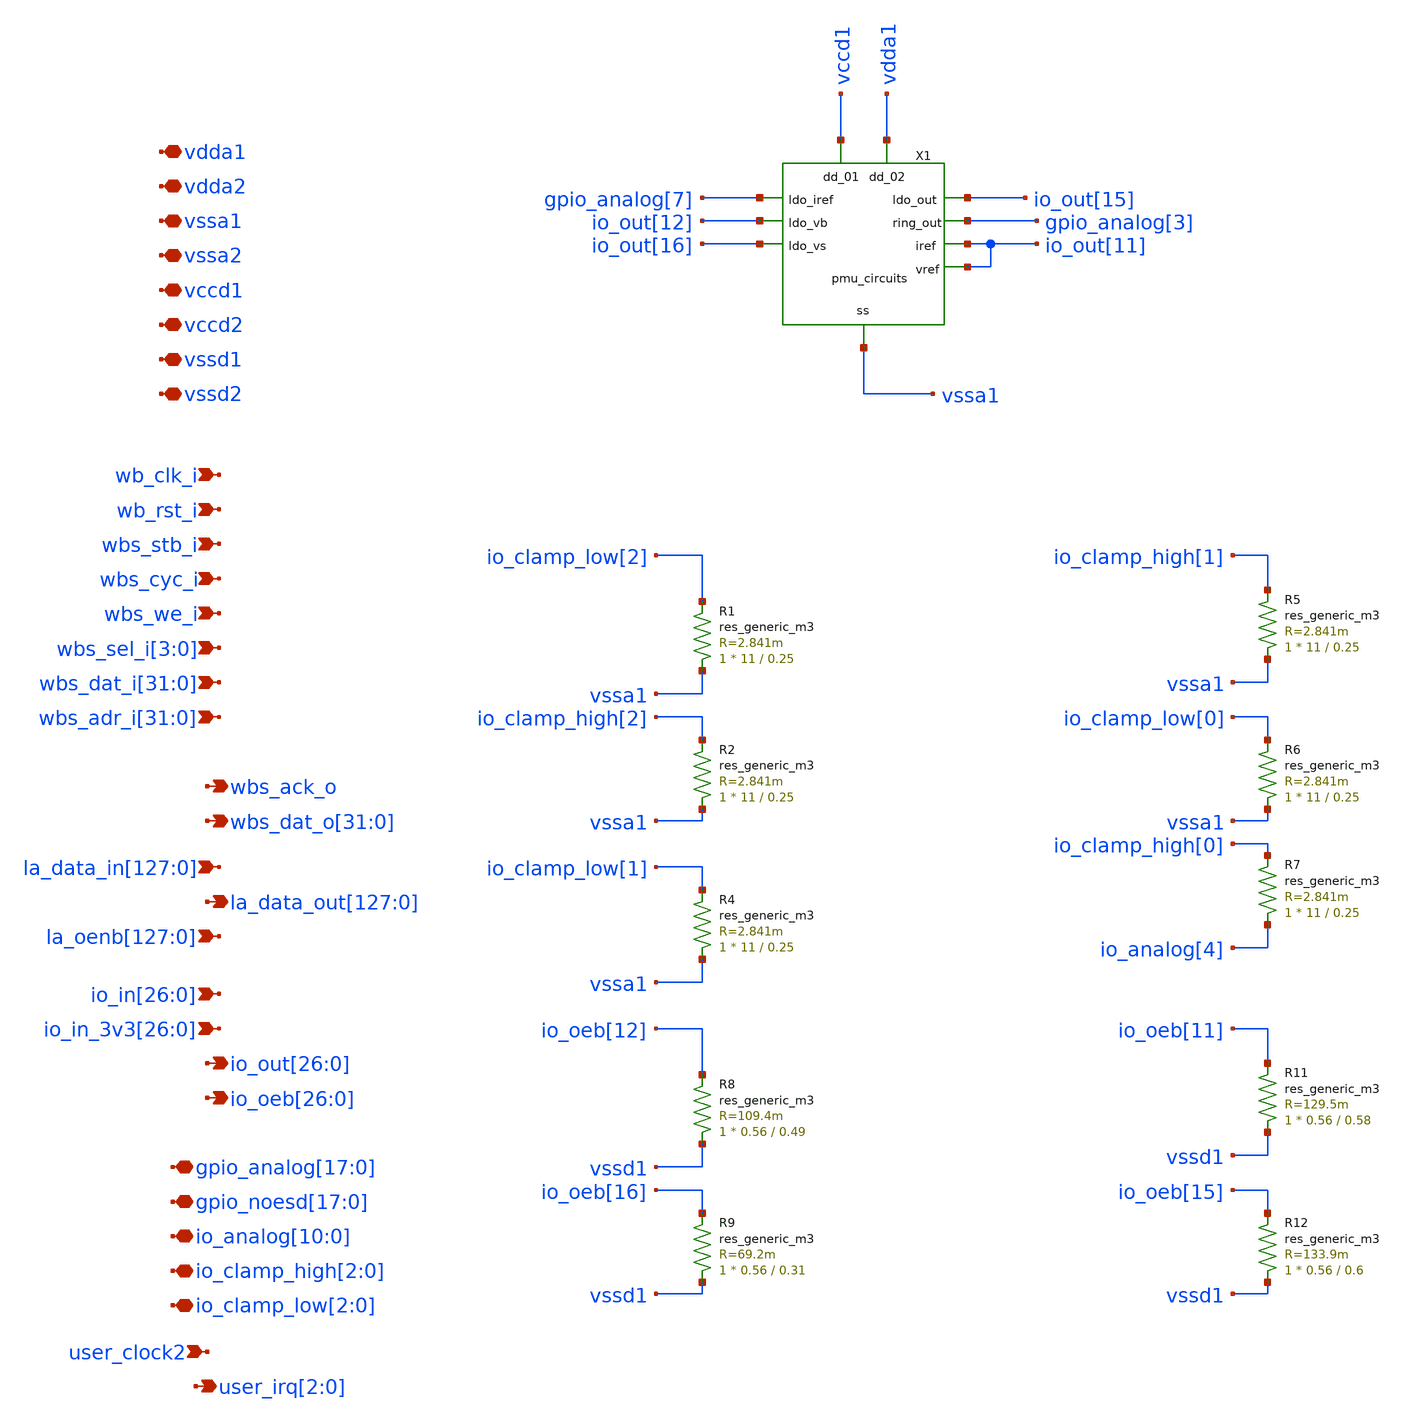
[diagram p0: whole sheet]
** sch_path: xschem/user_analog_project_wrapper.sch
**.subckt user_analog_project_wrapper vdda1 vdda2 vssa1 vssa2 vccd1 vccd2 vssd1 vssd2 wb_clk_i
*+ wb_rst_i wbs_stb_i wbs_cyc_i wbs_we_i wbs_sel_i[3],wbs_sel_i[2],wbs_sel_i[1],wbs_sel_i[0]
*+ wbs_dat_i[31],wbs_dat_i[30],wbs_dat_i[29],wbs_dat_i[28],wbs_dat_i[27],wbs_dat_i[26],wbs_dat_i[25],wbs_dat_i[24],wbs_dat_i[23],wbs_dat_i[22],wbs_dat_i[21],wbs_dat_i[20],wbs_dat_i[19],wbs_dat_i[18],wbs_dat_i[17],wbs_dat_i[16],wbs_dat_i[15],wbs_dat_i[14],wbs_dat_i[13],wbs_dat_i[12],wbs_dat_i[11],wbs_dat_i[10],wbs_dat_i[9],wbs_dat_i[8],wbs_dat_i[7],wbs_dat_i[6],wbs_dat_i[5],wbs_dat_i[4],wbs_dat_i[3],wbs_dat_i[2],wbs_dat_i[1],wbs_dat_i[0]
*+ wbs_adr_i[31],wbs_adr_i[30],wbs_adr_i[29],wbs_adr_i[28],wbs_adr_i[27],wbs_adr_i[26],wbs_adr_i[25],wbs_adr_i[24],wbs_adr_i[23],wbs_adr_i[22],wbs_adr_i[21],wbs_adr_i[20],wbs_adr_i[19],wbs_adr_i[18],wbs_adr_i[17],wbs_adr_i[16],wbs_adr_i[15],wbs_adr_i[14],wbs_adr_i[13],wbs_adr_i[12],wbs_adr_i[11],wbs_adr_i[10],wbs_adr_i[9],wbs_adr_i[8],wbs_adr_i[7],wbs_adr_i[6],wbs_adr_i[5],wbs_adr_i[4],wbs_adr_i[3],wbs_adr_i[2],wbs_adr_i[1],wbs_adr_i[0] wbs_ack_o
*+ wbs_dat_o[31],wbs_dat_o[30],wbs_dat_o[29],wbs_dat_o[28],wbs_dat_o[27],wbs_dat_o[26],wbs_dat_o[25],wbs_dat_o[24],wbs_dat_o[23],wbs_dat_o[22],wbs_dat_o[21],wbs_dat_o[20],wbs_dat_o[19],wbs_dat_o[18],wbs_dat_o[17],wbs_dat_o[16],wbs_dat_o[15],wbs_dat_o[14],wbs_dat_o[13],wbs_dat_o[12],wbs_dat_o[11],wbs_dat_o[10],wbs_dat_o[9],wbs_dat_o[8],wbs_dat_o[7],wbs_dat_o[6],wbs_dat_o[5],wbs_dat_o[4],wbs_dat_o[3],wbs_dat_o[2],wbs_dat_o[1],wbs_dat_o[0]
*+ la_data_in[127],la_data_in[126],la_data_in[125],la_data_in[124],la_data_in[123],la_data_in[122],la_data_in[121],la_data_in[120],la_data_in[119],la_data_in[118],la_data_in[117],la_data_in[116],la_data_in[115],la_data_in[114],la_data_in[113],la_data_in[112],la_data_in[111],la_data_in[110],la_data_in[109],la_data_in[108],la_data_in[107],la_data_in[106],la_data_in[105],la_data_in[104],la_data_in[103],la_data_in[102],la_data_in[101],la_data_in[100],la_data_in[99],la_data_in[98],la_data_in[97],la_data_in[96],la_data_in[95],la_data_in[94],la_data_in[93],la_data_in[92],la_data_in[91],la_data_in[90],la_data_in[89],la_data_in[88],la_data_in[87],la_data_in[86],la_data_in[85],la_data_in[84],la_data_in[83],la_data_in[82],la_data_in[81],la_data_in[80],la_data_in[79],la_data_in[78],la_data_in[77],la_data_in[76],la_data_in[75],la_data_in[74],la_data_in[73],la_data_in[72],la_data_in[71],la_data_in[70],la_data_in[69],la_data_in[68],la_data_in[67],la_data_in[66],la_data_in[65],la_data_in[64],la_data_in[63],la_data_in[62],la_data_in[61],la_data_in[60],la_data_in[59],la_data_in[58],la_data_in[57],la_data_in[56],la_data_in[55],la_data_in[54],la_data_in[53],la_data_in[52],la_data_in[51],la_data_in[50],la_data_in[49],la_data_in[48],la_data_in[47],la_data_in[46],la_data_in[45],la_data_in[44],la_data_in[43],la_data_in[42],la_data_in[41],la_data_in[40],la_data_in[39],la_data_in[38],la_data_in[37],la_data_in[36],la_data_in[35],la_data_in[34],la_data_in[33],la_data_in[32],la_data_in[31],la_data_in[30],la_data_in[29],la_data_in[28],la_data_in[27],la_data_in[26],la_data_in[25],la_data_in[24],la_data_in[23],la_data_in[22],la_data_in[21],la_data_in[20],la_data_in[19],la_data_in[18],la_data_in[17],la_data_in[16],la_data_in[15],la_data_in[14],la_data_in[13],la_data_in[12],la_data_in[11],la_data_in[10],la_data_in[9],la_data_in[8],la_data_in[7],la_data_in[6],la_data_in[5],la_data_in[4],la_data_in[3],la_data_in[2],la_data_in[1],la_data_in[0]
*+ la_data_out[127],la_data_out[126],la_data_out[125],la_data_out[124],la_data_out[123],la_data_out[122],la_data_out[121],la_data_out[120],la_data_out[119],la_data_out[118],la_data_out[117],la_data_out[116],la_data_out[115],la_data_out[114],la_data_out[113],la_data_out[112],la_data_out[111],la_data_out[110],la_data_out[109],la_data_out[108],la_data_out[107],la_data_out[106],la_data_out[105],la_data_out[104],la_data_out[103],la_data_out[102],la_data_out[101],la_data_out[100],la_data_out[99],la_data_out[98],la_data_out[97],la_data_out[96],la_data_out[95],la_data_out[94],la_data_out[93],la_data_out[92],la_data_out[91],la_data_out[90],la_data_out[89],la_data_out[88],la_data_out[87],la_data_out[86],la_data_out[85],la_data_out[84],la_data_out[83],la_data_out[82],la_data_out[81],la_data_out[80],la_data_out[79],la_data_out[78],la_data_out[77],la_data_out[76],la_data_out[75],la_data_out[74],la_data_out[73],la_data_out[72],la_data_out[71],la_data_out[70],la_data_out[69],la_data_out[68],la_data_out[67],la_data_out[66],la_data_out[65],la_data_out[64],la_data_out[63],la_data_out[62],la_data_out[61],la_data_out[60],la_data_out[59],la_data_out[58],la_data_out[57],la_data_out[56],la_data_out[55],la_data_out[54],la_data_out[53],la_data_out[52],la_data_out[51],la_data_out[50],la_data_out[49],la_data_out[48],la_data_out[47],la_data_out[46],la_data_out[45],la_data_out[44],la_data_out[43],la_data_out[42],la_data_out[41],la_data_out[40],la_data_out[39],la_data_out[38],la_data_out[37],la_data_out[36],la_data_out[35],la_data_out[34],la_data_out[33],la_data_out[32],la_data_out[31],la_data_out[30],la_data_out[29],la_data_out[28],la_data_out[27],la_data_out[26],la_data_out[25],la_data_out[24],la_data_out[23],la_data_out[22],la_data_out[21],la_data_out[20],la_data_out[19],la_data_out[18],la_data_out[17],la_data_out[16],la_data_out[15],la_data_out[14],la_data_out[13],la_data_out[12],la_data_out[11],la_data_out[10],la_data_out[9],la_data_out[8],la_data_out[7],la_data_out[6],la_data_out[5],la_data_out[4],la_data_out[3],la_data_out[2],la_data_out[1],la_data_out[0]
*+ io_in[26],io_in[25],io_in[24],io_in[23],io_in[22],io_in[21],io_in[20],io_in[19],io_in[18],io_in[17],io_in[16],io_in[15],io_in[14],io_in[13],io_in[12],io_in[11],io_in[10],io_in[9],io_in[8],io_in[7],io_in[6],io_in[5],io_in[4],io_in[3],io_in[2],io_in[1],io_in[0]
*+ io_in_3v3[26],io_in_3v3[25],io_in_3v3[24],io_in_3v3[23],io_in_3v3[22],io_in_3v3[21],io_in_3v3[20],io_in_3v3[19],io_in_3v3[18],io_in_3v3[17],io_in_3v3[16],io_in_3v3[15],io_in_3v3[14],io_in_3v3[13],io_in_3v3[12],io_in_3v3[11],io_in_3v3[10],io_in_3v3[9],io_in_3v3[8],io_in_3v3[7],io_in_3v3[6],io_in_3v3[5],io_in_3v3[4],io_in_3v3[3],io_in_3v3[2],io_in_3v3[1],io_in_3v3[0] user_clock2
*+ io_out[26],io_out[25],io_out[24],io_out[23],io_out[22],io_out[21],io_out[20],io_out[19],io_out[18],io_out[17],io_out[16],io_out[15],io_out[14],io_out[13],io_out[12],io_out[11],io_out[10],io_out[9],io_out[8],io_out[7],io_out[6],io_out[5],io_out[4],io_out[3],io_out[2],io_out[1],io_out[0]
*+ io_oeb[26],io_oeb[25],io_oeb[24],io_oeb[23],io_oeb[22],io_oeb[21],io_oeb[20],io_oeb[19],io_oeb[18],io_oeb[17],io_oeb[16],io_oeb[15],io_oeb[14],io_oeb[13],io_oeb[12],io_oeb[11],io_oeb[10],io_oeb[9],io_oeb[8],io_oeb[7],io_oeb[6],io_oeb[5],io_oeb[4],io_oeb[3],io_oeb[2],io_oeb[1],io_oeb[0]
*+ gpio_analog[17],gpio_analog[16],gpio_analog[15],gpio_analog[14],gpio_analog[13],gpio_analog[12],gpio_analog[11],gpio_analog[10],gpio_analog[9],gpio_analog[8],gpio_analog[7],gpio_analog[6],gpio_analog[5],gpio_analog[4],gpio_analog[3],gpio_analog[2],gpio_analog[1],gpio_analog[0]
*+ gpio_noesd[17],gpio_noesd[16],gpio_noesd[15],gpio_noesd[14],gpio_noesd[13],gpio_noesd[12],gpio_noesd[11],gpio_noesd[10],gpio_noesd[9],gpio_noesd[8],gpio_noesd[7],gpio_noesd[6],gpio_noesd[5],gpio_noesd[4],gpio_noesd[3],gpio_noesd[2],gpio_noesd[1],gpio_noesd[0]
*+ io_analog[10],io_analog[9],io_analog[8],io_analog[7],io_analog[6],io_analog[5],io_analog[4],io_analog[3],io_analog[2],io_analog[1],io_analog[0] io_clamp_high[2],io_clamp_high[1],io_clamp_high[0] io_clamp_low[2],io_clamp_low[1],io_clamp_low[0]
*+ user_irq[2],user_irq[1],user_irq[0]
*+ la_oenb[127],la_oenb[126],la_oenb[125],la_oenb[124],la_oenb[123],la_oenb[122],la_oenb[121],la_oenb[120],la_oenb[119],la_oenb[118],la_oenb[117],la_oenb[116],la_oenb[115],la_oenb[114],la_oenb[113],la_oenb[112],la_oenb[111],la_oenb[110],la_oenb[109],la_oenb[108],la_oenb[107],la_oenb[106],la_oenb[105],la_oenb[104],la_oenb[103],la_oenb[102],la_oenb[101],la_oenb[100],la_oenb[99],la_oenb[98],la_oenb[97],la_oenb[96],la_oenb[95],la_oenb[94],la_oenb[93],la_oenb[92],la_oenb[91],la_oenb[90],la_oenb[89],la_oenb[88],la_oenb[87],la_oenb[86],la_oenb[85],la_oenb[84],la_oenb[83],la_oenb[82],la_oenb[81],la_oenb[80],la_oenb[79],la_oenb[78],la_oenb[77],la_oenb[76],la_oenb[75],la_oenb[74],la_oenb[73],la_oenb[72],la_oenb[71],la_oenb[70],la_oenb[69],la_oenb[68],la_oenb[67],la_oenb[66],la_oenb[65],la_oenb[64],la_oenb[63],la_oenb[62],la_oenb[61],la_oenb[60],la_oenb[59],la_oenb[58],la_oenb[57],la_oenb[56],la_oenb[55],la_oenb[54],la_oenb[53],la_oenb[52],la_oenb[51],la_oenb[50],la_oenb[49],la_oenb[48],la_oenb[47],la_oenb[46],la_oenb[45],la_oenb[44],la_oenb[43],la_oenb[42],la_oenb[41],la_oenb[40],la_oenb[39],la_oenb[38],la_oenb[37],la_oenb[36],la_oenb[35],la_oenb[34],la_oenb[33],la_oenb[32],la_oenb[31],la_oenb[30],la_oenb[29],la_oenb[28],la_oenb[27],la_oenb[26],la_oenb[25],la_oenb[24],la_oenb[23],la_oenb[22],la_oenb[21],la_oenb[20],la_oenb[19],la_oenb[18],la_oenb[17],la_oenb[16],la_oenb[15],la_oenb[14],la_oenb[13],la_oenb[12],la_oenb[11],la_oenb[10],la_oenb[9],la_oenb[8],la_oenb[7],la_oenb[6],la_oenb[5],la_oenb[4],la_oenb[3],la_oenb[2],la_oenb[1],la_oenb[0]
*.iopin vdda1
*.iopin vdda2
*.iopin vssa1
*.iopin vssa2
*.iopin vccd1
*.iopin vccd2
*.iopin vssd1
*.iopin vssd2
*.ipin wb_clk_i
*.ipin wb_rst_i
*.ipin wbs_stb_i
*.ipin wbs_cyc_i
*.ipin wbs_we_i
*.ipin wbs_sel_i[3],wbs_sel_i[2],wbs_sel_i[1],wbs_sel_i[0]
*.ipin
*+ wbs_dat_i[31],wbs_dat_i[30],wbs_dat_i[29],wbs_dat_i[28],wbs_dat_i[27],wbs_dat_i[26],wbs_dat_i[25],wbs_dat_i[24],wbs_dat_i[23],wbs_dat_i[22],wbs_dat_i[21],wbs_dat_i[20],wbs_dat_i[19],wbs_dat_i[18],wbs_dat_i[17],wbs_dat_i[16],wbs_dat_i[15],wbs_dat_i[14],wbs_dat_i[13],wbs_dat_i[12],wbs_dat_i[11],wbs_dat_i[10],wbs_dat_i[9],wbs_dat_i[8],wbs_dat_i[7],wbs_dat_i[6],wbs_dat_i[5],wbs_dat_i[4],wbs_dat_i[3],wbs_dat_i[2],wbs_dat_i[1],wbs_dat_i[0]
*.ipin
*+ wbs_adr_i[31],wbs_adr_i[30],wbs_adr_i[29],wbs_adr_i[28],wbs_adr_i[27],wbs_adr_i[26],wbs_adr_i[25],wbs_adr_i[24],wbs_adr_i[23],wbs_adr_i[22],wbs_adr_i[21],wbs_adr_i[20],wbs_adr_i[19],wbs_adr_i[18],wbs_adr_i[17],wbs_adr_i[16],wbs_adr_i[15],wbs_adr_i[14],wbs_adr_i[13],wbs_adr_i[12],wbs_adr_i[11],wbs_adr_i[10],wbs_adr_i[9],wbs_adr_i[8],wbs_adr_i[7],wbs_adr_i[6],wbs_adr_i[5],wbs_adr_i[4],wbs_adr_i[3],wbs_adr_i[2],wbs_adr_i[1],wbs_adr_i[0]
*.opin wbs_ack_o
*.opin
*+ wbs_dat_o[31],wbs_dat_o[30],wbs_dat_o[29],wbs_dat_o[28],wbs_dat_o[27],wbs_dat_o[26],wbs_dat_o[25],wbs_dat_o[24],wbs_dat_o[23],wbs_dat_o[22],wbs_dat_o[21],wbs_dat_o[20],wbs_dat_o[19],wbs_dat_o[18],wbs_dat_o[17],wbs_dat_o[16],wbs_dat_o[15],wbs_dat_o[14],wbs_dat_o[13],wbs_dat_o[12],wbs_dat_o[11],wbs_dat_o[10],wbs_dat_o[9],wbs_dat_o[8],wbs_dat_o[7],wbs_dat_o[6],wbs_dat_o[5],wbs_dat_o[4],wbs_dat_o[3],wbs_dat_o[2],wbs_dat_o[1],wbs_dat_o[0]
*.ipin
*+ la_data_in[127],la_data_in[126],la_data_in[125],la_data_in[124],la_data_in[123],la_data_in[122],la_data_in[121],la_data_in[120],la_data_in[119],la_data_in[118],la_data_in[117],la_data_in[116],la_data_in[115],la_data_in[114],la_data_in[113],la_data_in[112],la_data_in[111],la_data_in[110],la_data_in[109],la_data_in[108],la_data_in[107],la_data_in[106],la_data_in[105],la_data_in[104],la_data_in[103],la_data_in[102],la_data_in[101],la_data_in[100],la_data_in[99],la_data_in[98],la_data_in[97],la_data_in[96],la_data_in[95],la_data_in[94],la_data_in[93],la_data_in[92],la_data_in[91],la_data_in[90],la_data_in[89],la_data_in[88],la_data_in[87],la_data_in[86],la_data_in[85],la_data_in[84],la_data_in[83],la_data_in[82],la_data_in[81],la_data_in[80],la_data_in[79],la_data_in[78],la_data_in[77],la_data_in[76],la_data_in[75],la_data_in[74],la_data_in[73],la_data_in[72],la_data_in[71],la_data_in[70],la_data_in[69],la_data_in[68],la_data_in[67],la_data_in[66],la_data_in[65],la_data_in[64],la_data_in[63],la_data_in[62],la_data_in[61],la_data_in[60],la_data_in[59],la_data_in[58],la_data_in[57],la_data_in[56],la_data_in[55],la_data_in[54],la_data_in[53],la_data_in[52],la_data_in[51],la_data_in[50],la_data_in[49],la_data_in[48],la_data_in[47],la_data_in[46],la_data_in[45],la_data_in[44],la_data_in[43],la_data_in[42],la_data_in[41],la_data_in[40],la_data_in[39],la_data_in[38],la_data_in[37],la_data_in[36],la_data_in[35],la_data_in[34],la_data_in[33],la_data_in[32],la_data_in[31],la_data_in[30],la_data_in[29],la_data_in[28],la_data_in[27],la_data_in[26],la_data_in[25],la_data_in[24],la_data_in[23],la_data_in[22],la_data_in[21],la_data_in[20],la_data_in[19],la_data_in[18],la_data_in[17],la_data_in[16],la_data_in[15],la_data_in[14],la_data_in[13],la_data_in[12],la_data_in[11],la_data_in[10],la_data_in[9],la_data_in[8],la_data_in[7],la_data_in[6],la_data_in[5],la_data_in[4],la_data_in[3],la_data_in[2],la_data_in[1],la_data_in[0]
*.opin
*+ la_data_out[127],la_data_out[126],la_data_out[125],la_data_out[124],la_data_out[123],la_data_out[122],la_data_out[121],la_data_out[120],la_data_out[119],la_data_out[118],la_data_out[117],la_data_out[116],la_data_out[115],la_data_out[114],la_data_out[113],la_data_out[112],la_data_out[111],la_data_out[110],la_data_out[109],la_data_out[108],la_data_out[107],la_data_out[106],la_data_out[105],la_data_out[104],la_data_out[103],la_data_out[102],la_data_out[101],la_data_out[100],la_data_out[99],la_data_out[98],la_data_out[97],la_data_out[96],la_data_out[95],la_data_out[94],la_data_out[93],la_data_out[92],la_data_out[91],la_data_out[90],la_data_out[89],la_data_out[88],la_data_out[87],la_data_out[86],la_data_out[85],la_data_out[84],la_data_out[83],la_data_out[82],la_data_out[81],la_data_out[80],la_data_out[79],la_data_out[78],la_data_out[77],la_data_out[76],la_data_out[75],la_data_out[74],la_data_out[73],la_data_out[72],la_data_out[71],la_data_out[70],la_data_out[69],la_data_out[68],la_data_out[67],la_data_out[66],la_data_out[65],la_data_out[64],la_data_out[63],la_data_out[62],la_data_out[61],la_data_out[60],la_data_out[59],la_data_out[58],la_data_out[57],la_data_out[56],la_data_out[55],la_data_out[54],la_data_out[53],la_data_out[52],la_data_out[51],la_data_out[50],la_data_out[49],la_data_out[48],la_data_out[47],la_data_out[46],la_data_out[45],la_data_out[44],la_data_out[43],la_data_out[42],la_data_out[41],la_data_out[40],la_data_out[39],la_data_out[38],la_data_out[37],la_data_out[36],la_data_out[35],la_data_out[34],la_data_out[33],la_data_out[32],la_data_out[31],la_data_out[30],la_data_out[29],la_data_out[28],la_data_out[27],la_data_out[26],la_data_out[25],la_data_out[24],la_data_out[23],la_data_out[22],la_data_out[21],la_data_out[20],la_data_out[19],la_data_out[18],la_data_out[17],la_data_out[16],la_data_out[15],la_data_out[14],la_data_out[13],la_data_out[12],la_data_out[11],la_data_out[10],la_data_out[9],la_data_out[8],la_data_out[7],la_data_out[6],la_data_out[5],la_data_out[4],la_data_out[3],la_data_out[2],la_data_out[1],la_data_out[0]
*.ipin
*+ io_in[26],io_in[25],io_in[24],io_in[23],io_in[22],io_in[21],io_in[20],io_in[19],io_in[18],io_in[17],io_in[16],io_in[15],io_in[14],io_in[13],io_in[12],io_in[11],io_in[10],io_in[9],io_in[8],io_in[7],io_in[6],io_in[5],io_in[4],io_in[3],io_in[2],io_in[1],io_in[0]
*.ipin
*+ io_in_3v3[26],io_in_3v3[25],io_in_3v3[24],io_in_3v3[23],io_in_3v3[22],io_in_3v3[21],io_in_3v3[20],io_in_3v3[19],io_in_3v3[18],io_in_3v3[17],io_in_3v3[16],io_in_3v3[15],io_in_3v3[14],io_in_3v3[13],io_in_3v3[12],io_in_3v3[11],io_in_3v3[10],io_in_3v3[9],io_in_3v3[8],io_in_3v3[7],io_in_3v3[6],io_in_3v3[5],io_in_3v3[4],io_in_3v3[3],io_in_3v3[2],io_in_3v3[1],io_in_3v3[0]
*.ipin user_clock2
*.opin
*+ io_out[26],io_out[25],io_out[24],io_out[23],io_out[22],io_out[21],io_out[20],io_out[19],io_out[18],io_out[17],io_out[16],io_out[15],io_out[14],io_out[13],io_out[12],io_out[11],io_out[10],io_out[9],io_out[8],io_out[7],io_out[6],io_out[5],io_out[4],io_out[3],io_out[2],io_out[1],io_out[0]
*.opin
*+ io_oeb[26],io_oeb[25],io_oeb[24],io_oeb[23],io_oeb[22],io_oeb[21],io_oeb[20],io_oeb[19],io_oeb[18],io_oeb[17],io_oeb[16],io_oeb[15],io_oeb[14],io_oeb[13],io_oeb[12],io_oeb[11],io_oeb[10],io_oeb[9],io_oeb[8],io_oeb[7],io_oeb[6],io_oeb[5],io_oeb[4],io_oeb[3],io_oeb[2],io_oeb[1],io_oeb[0]
*.iopin
*+ gpio_analog[17],gpio_analog[16],gpio_analog[15],gpio_analog[14],gpio_analog[13],gpio_analog[12],gpio_analog[11],gpio_analog[10],gpio_analog[9],gpio_analog[8],gpio_analog[7],gpio_analog[6],gpio_analog[5],gpio_analog[4],gpio_analog[3],gpio_analog[2],gpio_analog[1],gpio_analog[0]
*.iopin
*+ gpio_noesd[17],gpio_noesd[16],gpio_noesd[15],gpio_noesd[14],gpio_noesd[13],gpio_noesd[12],gpio_noesd[11],gpio_noesd[10],gpio_noesd[9],gpio_noesd[8],gpio_noesd[7],gpio_noesd[6],gpio_noesd[5],gpio_noesd[4],gpio_noesd[3],gpio_noesd[2],gpio_noesd[1],gpio_noesd[0]
*.iopin
*+ io_analog[10],io_analog[9],io_analog[8],io_analog[7],io_analog[6],io_analog[5],io_analog[4],io_analog[3],io_analog[2],io_analog[1],io_analog[0]
*.iopin io_clamp_high[2],io_clamp_high[1],io_clamp_high[0]
*.iopin io_clamp_low[2],io_clamp_low[1],io_clamp_low[0]
*.opin user_irq[2],user_irq[1],user_irq[0]
*.ipin
*+ la_oenb[127],la_oenb[126],la_oenb[125],la_oenb[124],la_oenb[123],la_oenb[122],la_oenb[121],la_oenb[120],la_oenb[119],la_oenb[118],la_oenb[117],la_oenb[116],la_oenb[115],la_oenb[114],la_oenb[113],la_oenb[112],la_oenb[111],la_oenb[110],la_oenb[109],la_oenb[108],la_oenb[107],la_oenb[106],la_oenb[105],la_oenb[104],la_oenb[103],la_oenb[102],la_oenb[101],la_oenb[100],la_oenb[99],la_oenb[98],la_oenb[97],la_oenb[96],la_oenb[95],la_oenb[94],la_oenb[93],la_oenb[92],la_oenb[91],la_oenb[90],la_oenb[89],la_oenb[88],la_oenb[87],la_oenb[86],la_oenb[85],la_oenb[84],la_oenb[83],la_oenb[82],la_oenb[81],la_oenb[80],la_oenb[79],la_oenb[78],la_oenb[77],la_oenb[76],la_oenb[75],la_oenb[74],la_oenb[73],la_oenb[72],la_oenb[71],la_oenb[70],la_oenb[69],la_oenb[68],la_oenb[67],la_oenb[66],la_oenb[65],la_oenb[64],la_oenb[63],la_oenb[62],la_oenb[61],la_oenb[60],la_oenb[59],la_oenb[58],la_oenb[57],la_oenb[56],la_oenb[55],la_oenb[54],la_oenb[53],la_oenb[52],la_oenb[51],la_oenb[50],la_oenb[49],la_oenb[48],la_oenb[47],la_oenb[46],la_oenb[45],la_oenb[44],la_oenb[43],la_oenb[42],la_oenb[41],la_oenb[40],la_oenb[39],la_oenb[38],la_oenb[37],la_oenb[36],la_oenb[35],la_oenb[34],la_oenb[33],la_oenb[32],la_oenb[31],la_oenb[30],la_oenb[29],la_oenb[28],la_oenb[27],la_oenb[26],la_oenb[25],la_oenb[24],la_oenb[23],la_oenb[22],la_oenb[21],la_oenb[20],la_oenb[19],la_oenb[18],la_oenb[17],la_oenb[16],la_oenb[15],la_oenb[14],la_oenb[13],la_oenb[12],la_oenb[11],la_oenb[10],la_oenb[9],la_oenb[8],la_oenb[7],la_oenb[6],la_oenb[5],la_oenb[4],la_oenb[3],la_oenb[2],la_oenb[1],la_oenb[0]
R1 vssa1 io_clamp_low[2] sky130_fd_pr__res_generic_m3 W=11 L=0.25 m=1
R2 vssa1 io_clamp_high[2] sky130_fd_pr__res_generic_m3 W=11 L=0.25 m=1
R4 vssa1 io_clamp_low[1] sky130_fd_pr__res_generic_m3 W=11 L=0.25 m=1
R5 vssa1 io_clamp_high[1] sky130_fd_pr__res_generic_m3 W=11 L=0.25 m=1
R6 vssa1 io_clamp_low[0] sky130_fd_pr__res_generic_m3 W=11 L=0.25 m=1
R7 io_analog[4] io_clamp_high[0] sky130_fd_pr__res_generic_m3 W=11 L=0.25 m=1
R8 vssd1 io_oeb[12] sky130_fd_pr__res_generic_m3 W=0.56 L=0.49 m=1
R9 vssd1 io_oeb[16] sky130_fd_pr__res_generic_m3 W=0.56 L=0.31 m=1
R11 vssd1 io_oeb[11] sky130_fd_pr__res_generic_m3 W=0.56 L=0.58 m=1
R12 vssd1 io_oeb[15] sky130_fd_pr__res_generic_m3 W=0.56 L=0.6 m=1
X1 gpio_analog[7] io_out[12] io_out[16] io_out[15] gpio_analog[3] io_out[11] io_out[11] vccd1 vdda1
+ vssa1 pmu_circuits
**.ends

* expanding   symbol:  pmu_circuits.sym # of pins=10
** sym_path: xschem/pmu_circuits.sym
** sch_path: xschem/pmu_circuits.sch
.subckt pmu_circuits ldo_iref ldo_vb ldo_vs ldo_out ring_out iref vref dd_01 dd_02 ss
*.iopin dd_01
*.iopin dd_02
*.iopin ss
*.opin ldo_out
*.opin ring_out
*.opin iref
*.opin vref
*.ipin ldo_iref
*.ipin ldo_vb
*.ipin ldo_vs
x2 ring_out dd_02 ss ring_100mV
x1 ldo_out dd_01 ss ldo_vb ldo_vs ldo_iref ldo
x3 iref dd_01 ss iref_2nA
x4 vref dd_01 ss vref01
.ends


* expanding   symbol:  ring_100mV.sym # of pins=3
** sym_path: xschem/ring_100mV.sym
** sch_path: xschem/ring_100mV.sch
.subckt ring_100mV OUT DD SS
*.iopin DD
*.iopin SS
*.opin OUT
X2 net1 net2 DD SS mdls_inv
X1 net2 net3 DD SS mdls_inv
X3 net3 net4 DD SS mdls_inv
X4 net4 out_aux DD SS mdls_inv
X10 out_aux net5 DD SS mdls_inv
X11 net5 net6 DD SS mdls_inv
X12 net6 net7 DD SS mdls_inv
X13 net7 net8 DD SS mdls_inv
X14 net8 net1 DD SS mdls_inv
X5 out_aux net9 DD SS mdls_inv
X6 net9 OUT DD SS ring_100mV_buffer
.ends


* expanding   symbol:  ldo.sym # of pins=6
** sym_path: xschem/ldo.sym
** sch_path: xschem/ldo.sch
.subckt ldo OUT DD SS VB VS Iref
*.iopin DD
*.ipin Iref
*.opin OUT
*.ipin VB
*.ipin VS
*.iopin SS
XMN1 net3 VB net1 SS sky130_fd_pr__nfet_01v8_lvt L=1.43 W=5.19 nf=1 ad='int((nf+1)/2) * W/nf * 0.29'
+ as='int((nf+2)/2) * W/nf * 0.29' pd='2*int((nf+1)/2) * (W/nf + 0.29)' ps='2*int((nf+2)/2) * (W/nf + 0.29)'
+ nrd='0.29 / W' nrs='0.29 / W' sa=0 sb=0 sd=0 mult=2 m=2
XMN2c net1 Iref SS SS sky130_fd_pr__nfet_01v8_lvt L=0.66 W=5.10 nf=1 ad='int((nf+1)/2) * W/nf * 0.29'
+ as='int((nf+2)/2) * W/nf * 0.29' pd='2*int((nf+1)/2) * (W/nf + 0.29)' ps='2*int((nf+2)/2) * (W/nf + 0.29)'
+ nrd='0.29 / W' nrs='0.29 / W' sa=0 sb=0 sd=0 mult=4 m=4
XMN2b net2 Iref SS SS sky130_fd_pr__nfet_01v8_lvt L=0.66 W=5.10 nf=1 ad='int((nf+1)/2) * W/nf * 0.29'
+ as='int((nf+2)/2) * W/nf * 0.29' pd='2*int((nf+1)/2) * (W/nf + 0.29)' ps='2*int((nf+2)/2) * (W/nf + 0.29)'
+ nrd='0.29 / W' nrs='0.29 / W' sa=0 sb=0 sd=0 mult=2 m=2
XMN2a Iref Iref SS SS sky130_fd_pr__nfet_01v8_lvt L=0.66 W=5.10 nf=1 ad='int((nf+1)/2) * W/nf * 0.29'
+ as='int((nf+2)/2) * W/nf * 0.29' pd='2*int((nf+1)/2) * (W/nf + 0.29)' ps='2*int((nf+2)/2) * (W/nf + 0.29)'
+ nrd='0.29 / W' nrs='0.29 / W' sa=0 sb=0 sd=0 mult=2 m=2
XMP2 net1 VS OUT OUT sky130_fd_pr__pfet_01v8_lvt L=1.27 W=6.07 nf=1 ad='int((nf+1)/2) * W/nf * 0.29'
+ as='int((nf+2)/2) * W/nf * 0.29' pd='2*int((nf+1)/2) * (W/nf + 0.29)' ps='2*int((nf+2)/2) * (W/nf + 0.29)'
+ nrd='0.29 / W' nrs='0.29 / W' sa=0 sb=0 sd=0 mult=2 m=2
XMP1 OUT net3 DD DD sky130_fd_pr__pfet_01v8_lvt L=0.37 W=5.17 nf=1 ad='int((1 + 1)/2) * 5.17 / 1 * 0.29'
+ as='int((1 + 2)/2) * 5.17 / 1 * 0.29' pd='2*int((1 + 1)/2) * (5.17 / 1 + 0.29)' ps='2*int((1 + 2)/2) * (5.17 / 1 + 0.29)'
+ nrd='0.29 / 5.17 ' nrs='0.29 / 5.17 ' sa=0 sb=0 sd=0 mult=1 m=1
XMP3b net3 net2 DD DD sky130_fd_pr__pfet_01v8 L=3.89 W=0.89 nf=1 ad='int((nf+1)/2) * W/nf * 0.29' as='int((nf+2)/2) * W/nf * 0.29'
+ pd='2*int((nf+1)/2) * (W/nf + 0.29)' ps='2*int((nf+2)/2) * (W/nf + 0.29)' nrd='0.29 / W' nrs='0.29 / W'
+ sa=0 sb=0 sd=0 mult=2 m=2
XMP3a net2 net2 DD DD sky130_fd_pr__pfet_01v8 L=3.89 W=0.89 nf=1 ad='int((nf+1)/2) * W/nf * 0.29' as='int((nf+2)/2) * W/nf * 0.29'
+ pd='2*int((nf+1)/2) * (W/nf + 0.29)' ps='2*int((nf+2)/2) * (W/nf + 0.29)' nrd='0.29 / W' nrs='0.29 / W'
+ sa=0 sb=0 sd=0 mult=2 m=2
XC1 net3 OUT sky130_fd_pr__cap_mim_m3_1 W=4 L=15 MF=1 m=1
XMP3 DD DD DD DD sky130_fd_pr__pfet_01v8 L=3.89 W=0.89 nf=1 ad='int((nf+1)/2) * W/nf * 0.29' as='int((nf+2)/2) * W/nf * 0.29'
+ pd='2*int((nf+1)/2) * (W/nf + 0.29)' ps='2*int((nf+2)/2) * (W/nf + 0.29)' nrd='0.29 / W' nrs='0.29 / W'
+ sa=0 sb=0 sd=0 mult=2 m=2
XMN2 SS SS SS SS sky130_fd_pr__nfet_01v8_lvt L=0.66 W=5.10 nf=1 ad='int((nf+1)/2) * W/nf * 0.29' as='int((nf+2)/2) * W/nf * 0.29'
+ pd='2*int((nf+1)/2) * (W/nf + 0.29)' ps='2*int((nf+2)/2) * (W/nf + 0.29)' nrd='0.29 / W' nrs='0.29 / W'
+ sa=0 sb=0 sd=0 mult=2 m=2
.ends


* expanding   symbol:  iref_2nA.sym # of pins=3
** sym_path: xschem/iref_2nA.sym
** sch_path: xschem/iref_2nA.sch
.subckt iref_2nA IREF DD SS
*.iopin DD
*.iopin SS
*.iopin IREF
x1 net3 SS net1 VCTAT net2 iref_2nA_igenerator
x3 DD SS net1 net2 net3 IREF iref_2nA_mirrors
x2 VCTAT DD SS iref_2nA_vref
.ends


* expanding   symbol:  vref01.sym # of pins=3
** sym_path: xschem/vref01.sym
** sch_path: xschem/vref01.sch
.subckt vref01 VREF DD SS
*.opin VREF
*.iopin SS
*.iopin DD
XM1 DD gate gate SS sky130_fd_pr__nfet_01v8_lvt L=0.89 W=6 nf=1 ad='int((nf+1)/2) * W/nf * 0.29' as='int((nf+2)/2) * W/nf * 0.29'
+ pd='2*int((nf+1)/2) * (W/nf + 0.29)' ps='2*int((nf+2)/2) * (W/nf + 0.29)' nrd='0.29 / W' nrs='0.29 / W'
+ sa=0 sb=0 sd=0 mult=2 m=2
XM2 gate gate VREF SS sky130_fd_pr__nfet_01v8_lvt L=3.10 W=1.72 nf=1 ad='int((nf+1)/2) * W/nf * 0.29'
+ as='int((nf+2)/2) * W/nf * 0.29' pd='2*int((nf+1)/2) * (W/nf + 0.29)' ps='2*int((nf+2)/2) * (W/nf + 0.29)'
+ nrd='0.29 / W' nrs='0.29 / W' sa=0 sb=0 sd=0 mult=1 m=1
XM3 VREF gate SS SS sky130_fd_pr__nfet_01v8 L=1.05 W=0.82 nf=1 ad='int((nf+1)/2) * W/nf * 0.29' as='int((nf+2)/2) * W/nf * 0.29'
+ pd='2*int((nf+1)/2) * (W/nf + 0.29)' ps='2*int((nf+2)/2) * (W/nf + 0.29)' nrd='0.29 / W' nrs='0.29 / W'
+ sa=0 sb=0 sd=0 mult=1 m=1
D1 VREF DD sky130_fd_pr__diode_pd2nw_05v5_lvt area=4.225e+11
.ends


* expanding   symbol:  mdls_inv.sym # of pins=4
** sym_path: xschem/mdls_inv.sym
** sch_path: xschem/mdls_inv.sch
.subckt mdls_inv IN OUT DD SS
*.ipin IN
*.iopin DD
*.iopin SS
*.opin OUT
XM5 OUT IN net1 SS sky130_fd_pr__nfet_01v8_lvt L=0.8 W=5.5 nf=1 ad='int((nf+1)/2) * W/nf * 0.29' as='int((nf+2)/2) * W/nf * 0.29'
+ pd='2*int((nf+1)/2) * (W/nf + 0.29)' ps='2*int((nf+2)/2) * (W/nf + 0.29)' nrd='0.29 / W' nrs='0.29 / W'
+ sa=0 sb=0 sd=0 mult=4 m=4
XM10 OUT IN net2 DD sky130_fd_pr__pfet_01v8_lvt L=0.8 W=1 nf=1 ad='int((nf+1)/2) * W/nf * 0.29' as='int((nf+2)/2) * W/nf * 0.29'
+ pd='2*int((nf+1)/2) * (W/nf + 0.29)' ps='2*int((nf+2)/2) * (W/nf + 0.29)' nrd='0.29 / W' nrs='0.29 / W'
+ sa=0 sb=0 sd=0 mult=1 m=1
XM11 net1 IN SS SS sky130_fd_pr__nfet_01v8_lvt L=1 W=5.5 nf=1 ad='int((nf+1)/2) * W/nf * 0.29' as='int((nf+2)/2) * W/nf * 0.29'
+ pd='2*int((nf+1)/2) * (W/nf + 0.29)' ps='2*int((nf+2)/2) * (W/nf + 0.29)' nrd='0.29 / W' nrs='0.29 / W'
+ sa=0 sb=0 sd=0 mult=2 m=2
XM13 net2 IN DD DD sky130_fd_pr__pfet_01v8_lvt L=2 W=1 nf=1 ad='int((nf+1)/2) * W/nf * 0.29' as='int((nf+2)/2) * W/nf * 0.29'
+ pd='2*int((nf+1)/2) * (W/nf + 0.29)' ps='2*int((nf+2)/2) * (W/nf + 0.29)' nrd='0.29 / W' nrs='0.29 / W'
+ sa=0 sb=0 sd=0 mult=1 m=1
XM1 net1 OUT SS DD sky130_fd_pr__pfet_01v8_lvt L=0.8 W=1 nf=1 ad='int((nf+1)/2) * W/nf * 0.29' as='int((nf+2)/2) * W/nf * 0.29'
+ pd='2*int((nf+1)/2) * (W/nf + 0.29)' ps='2*int((nf+2)/2) * (W/nf + 0.29)' nrd='0.29 / W' nrs='0.29 / W'
+ sa=0 sb=0 sd=0 mult=1 m=1
XM2 net2 OUT DD SS sky130_fd_pr__nfet_01v8_lvt L=0.4 W=5.5 nf=1 ad='int((nf+1)/2) * W/nf * 0.29' as='int((nf+2)/2) * W/nf * 0.29'
+ pd='2*int((nf+1)/2) * (W/nf + 0.29)' ps='2*int((nf+2)/2) * (W/nf + 0.29)' nrd='0.29 / W' nrs='0.29 / W'
+ sa=0 sb=0 sd=0 mult=2 m=2
.ends


* expanding   symbol:  ring_100mV_buffer.sym # of pins=4
** sym_path: xschem/ring_100mV_buffer.sym
** sch_path: xschem/ring_100mV_buffer.sch
.subckt ring_100mV_buffer IN OUT DD SS
*.opin OUT
*.iopin DD
*.iopin SS
*.ipin IN
XM5 net1 IN SS SS sky130_fd_pr__nfet_01v8_lvt L=0.8 W=5.5 nf=1 ad='int((nf+1)/2) * W/nf * 0.29' as='int((nf+2)/2) * W/nf * 0.29'
+ pd='2*int((nf+1)/2) * (W/nf + 0.29)' ps='2*int((nf+2)/2) * (W/nf + 0.29)' nrd='0.29 / W' nrs='0.29 / W'
+ sa=0 sb=0 sd=0 mult=8 m=8
XM10 net1 IN DD DD sky130_fd_pr__pfet_01v8_lvt L=0.8 W=1 nf=1 ad='int((nf+1)/2) * W/nf * 0.29' as='int((nf+2)/2) * W/nf * 0.29'
+ pd='2*int((nf+1)/2) * (W/nf + 0.29)' ps='2*int((nf+2)/2) * (W/nf + 0.29)' nrd='0.29 / W' nrs='0.29 / W'
+ sa=0 sb=0 sd=0 mult=2 m=2
XM1 OUT net1 SS SS sky130_fd_pr__nfet_01v8_lvt L=0.8 W=5.5 nf=1 ad='int((nf+1)/2) * W/nf * 0.29' as='int((nf+2)/2) * W/nf * 0.29'
+ pd='2*int((nf+1)/2) * (W/nf + 0.29)' ps='2*int((nf+2)/2) * (W/nf + 0.29)' nrd='0.29 / W' nrs='0.29 / W'
+ sa=0 sb=0 sd=0 mult=16 m=16
XM2 OUT net1 DD DD sky130_fd_pr__pfet_01v8_lvt L=0.8 W=1 nf=1 ad='int((nf+1)/2) * W/nf * 0.29' as='int((nf+2)/2) * W/nf * 0.29'
+ pd='2*int((nf+1)/2) * (W/nf + 0.29)' ps='2*int((nf+2)/2) * (W/nf + 0.29)' nrd='0.29 / W' nrs='0.29 / W'
+ sa=0 sb=0 sd=0 mult=4 m=4
.ends


* expanding   symbol:  iref_2nA_igenerator.sym # of pins=5
** sym_path: xschem/iref_2nA_igenerator.sym
** sch_path: xschem/iref_2nA_igenerator.sch
.subckt iref_2nA_igenerator Ip2 SS Ip1 VCTAT Vg
*.iopin SS
*.ipin VCTAT
*.iopin Ip1
*.iopin Vg
*.iopin Ip2
XM1 Ip1 Vg VPTAT SS sky130_fd_pr__nfet_01v8_lvt L=1 W=2.5 nf=1 ad='int((nf+1)/2) * W/nf * 0.29' as='int((nf+2)/2) * W/nf * 0.29'
+ pd='2*int((nf+1)/2) * (W/nf + 0.29)' ps='2*int((nf+2)/2) * (W/nf + 0.29)' nrd='0.29 / W' nrs='0.29 / W'
+ sa=0 sb=0 sd=0 mult=2 m=2
XM2 Ip2 Vg SS SS sky130_fd_pr__nfet_01v8_lvt L=1 W=2.5 nf=1 ad='int((nf+1)/2) * W/nf * 0.29' as='int((nf+2)/2) * W/nf * 0.29'
+ pd='2*int((nf+1)/2) * (W/nf + 0.29)' ps='2*int((nf+2)/2) * (W/nf + 0.29)' nrd='0.29 / W' nrs='0.29 / W'
+ sa=0 sb=0 sd=0 mult=2 m=2
XM3 VPTAT VCTAT SS SS sky130_fd_pr__nfet_01v8_lvt L=5 W=1 nf=1 ad='int((nf+1)/2) * W/nf * 0.29' as='int((nf+2)/2) * W/nf * 0.29'
+ pd='2*int((nf+1)/2) * (W/nf + 0.29)' ps='2*int((nf+2)/2) * (W/nf + 0.29)' nrd='0.29 / W' nrs='0.29 / W'
+ sa=0 sb=0 sd=0 mult=1 m=1
XM4 SS SS SS SS sky130_fd_pr__nfet_01v8_lvt L=1 W=2.5 nf=1 ad='int((nf+1)/2) * W/nf * 0.29' as='int((nf+2)/2) * W/nf * 0.29'
+ pd='2*int((nf+1)/2) * (W/nf + 0.29)' ps='2*int((nf+2)/2) * (W/nf + 0.29)' nrd='0.29 / W' nrs='0.29 / W'
+ sa=0 sb=0 sd=0 mult=2 m=2
.ends


* expanding   symbol:  iref_2nA_mirrors.sym # of pins=6
** sym_path: xschem/iref_2nA_mirrors.sym
** sch_path: xschem/iref_2nA_mirrors.sch
.subckt iref_2nA_mirrors DD SS Ip1 Vg Ip2 Iref
*.iopin DD
*.iopin SS
*.iopin Iref
*.iopin Ip2
*.iopin Vg
*.iopin Ip1
XM7 net3 Ip2 DD DD sky130_fd_pr__pfet_01v8_lvt L=2 W=2.5 nf=1 ad='int((nf+1)/2) * W/nf * 0.29' as='int((nf+2)/2) * W/nf * 0.29'
+ pd='2*int((nf+1)/2) * (W/nf + 0.29)' ps='2*int((nf+2)/2) * (W/nf + 0.29)' nrd='0.29 / W' nrs='0.29 / W'
+ sa=0 sb=0 sd=0 mult=10 m=10
XM8 net2 Ip1 DD DD sky130_fd_pr__pfet_01v8_lvt L=2 W=2.5 nf=1 ad='int((nf+1)/2) * W/nf * 0.29' as='int((nf+2)/2) * W/nf * 0.29'
+ pd='2*int((nf+1)/2) * (W/nf + 0.29)' ps='2*int((nf+2)/2) * (W/nf + 0.29)' nrd='0.29 / W' nrs='0.29 / W'
+ sa=0 sb=0 sd=0 mult=2 m=2
XM9 net4 Ip2 DD DD sky130_fd_pr__pfet_01v8_lvt L=2 W=2.5 nf=1 ad='int((nf+1)/2) * W/nf * 0.29' as='int((nf+2)/2) * W/nf * 0.29'
+ pd='2*int((nf+1)/2) * (W/nf + 0.29)' ps='2*int((nf+2)/2) * (W/nf + 0.29)' nrd='0.29 / W' nrs='0.29 / W'
+ sa=0 sb=0 sd=0 mult=2 m=2
XM10 net1 Ip1 DD DD sky130_fd_pr__pfet_01v8_lvt L=2 W=2.5 nf=1 ad='int((nf+1)/2) * W/nf * 0.29' as='int((nf+2)/2) * W/nf * 0.29'
+ pd='2*int((nf+1)/2) * (W/nf + 0.29)' ps='2*int((nf+2)/2) * (W/nf + 0.29)' nrd='0.29 / W' nrs='0.29 / W'
+ sa=0 sb=0 sd=0 mult=2 m=2
XM11 Vn Vn SS SS sky130_fd_pr__nfet_01v8_lvt L=1 W=2.5 nf=1 ad='int((nf+1)/2) * W/nf * 0.29' as='int((nf+2)/2) * W/nf * 0.29'
+ pd='2*int((nf+1)/2) * (W/nf + 0.29)' ps='2*int((nf+2)/2) * (W/nf + 0.29)' nrd='0.29 / W' nrs='0.29 / W'
+ sa=0 sb=0 sd=0 mult=2 m=2
XM12 Vg Vn SS SS sky130_fd_pr__nfet_01v8_lvt L=1 W=2.5 nf=1 ad='int((nf+1)/2) * W/nf * 0.29' as='int((nf+2)/2) * W/nf * 0.29'
+ pd='2*int((nf+1)/2) * (W/nf + 0.29)' ps='2*int((nf+2)/2) * (W/nf + 0.29)' nrd='0.29 / W' nrs='0.29 / W'
+ sa=0 sb=0 sd=0 mult=2 m=2
XM15 net5 Ip2 DD DD sky130_fd_pr__pfet_01v8_lvt L=2 W=2.5 nf=1 ad='int((nf+1)/2) * W/nf * 0.29' as='int((nf+2)/2) * W/nf * 0.29'
+ pd='2*int((nf+1)/2) * (W/nf + 0.29)' ps='2*int((nf+2)/2) * (W/nf + 0.29)' nrd='0.29 / W' nrs='0.29 / W'
+ sa=0 sb=0 sd=0 mult=2 m=2
XM16 Vg Vb net2 DD sky130_fd_pr__pfet_01v8_lvt L=2 W=2.5 nf=1 ad='int((nf+1)/2) * W/nf * 0.29' as='int((nf+2)/2) * W/nf * 0.29'
+ pd='2*int((nf+1)/2) * (W/nf + 0.29)' ps='2*int((nf+2)/2) * (W/nf + 0.29)' nrd='0.29 / W' nrs='0.29 / W'
+ sa=0 sb=0 sd=0 mult=2 m=2
XM17 Ip1 Vb net1 DD sky130_fd_pr__pfet_01v8_lvt L=2 W=2.5 nf=1 ad='int((nf+1)/2) * W/nf * 0.29' as='int((nf+2)/2) * W/nf * 0.29'
+ pd='2*int((nf+1)/2) * (W/nf + 0.29)' ps='2*int((nf+2)/2) * (W/nf + 0.29)' nrd='0.29 / W' nrs='0.29 / W'
+ sa=0 sb=0 sd=0 mult=2 m=2
XM18 Ip2 Vb net3 DD sky130_fd_pr__pfet_01v8_lvt L=2 W=2.5 nf=1 ad='int((nf+1)/2) * W/nf * 0.29' as='int((nf+2)/2) * W/nf * 0.29'
+ pd='2*int((nf+1)/2) * (W/nf + 0.29)' ps='2*int((nf+2)/2) * (W/nf + 0.29)' nrd='0.29 / W' nrs='0.29 / W'
+ sa=0 sb=0 sd=0 mult=10 m=10
XM19 Vn Vb net4 DD sky130_fd_pr__pfet_01v8_lvt L=2 W=2.5 nf=1 ad='int((nf+1)/2) * W/nf * 0.29' as='int((nf+2)/2) * W/nf * 0.29'
+ pd='2*int((nf+1)/2) * (W/nf + 0.29)' ps='2*int((nf+2)/2) * (W/nf + 0.29)' nrd='0.29 / W' nrs='0.29 / W'
+ sa=0 sb=0 sd=0 mult=2 m=2
XM20 Iref Vb net5 DD sky130_fd_pr__pfet_01v8_lvt L=2 W=2.5 nf=1 ad='int((nf+1)/2) * W/nf * 0.29' as='int((nf+2)/2) * W/nf * 0.29'
+ pd='2*int((nf+1)/2) * (W/nf + 0.29)' ps='2*int((nf+2)/2) * (W/nf + 0.29)' nrd='0.29 / W' nrs='0.29 / W'
+ sa=0 sb=0 sd=0 mult=2 m=2
XM22 net6 net6 DD DD sky130_fd_pr__pfet_01v8_lvt L=2 W=2.5 nf=1 ad='int((nf+1)/2) * W/nf * 0.29' as='int((nf+2)/2) * W/nf * 0.29'
+ pd='2*int((nf+1)/2) * (W/nf + 0.29)' ps='2*int((nf+2)/2) * (W/nf + 0.29)' nrd='0.29 / W' nrs='0.29 / W'
+ sa=0 sb=0 sd=0 mult=2 m=2
XM21 Vb Vn SS SS sky130_fd_pr__nfet_01v8_lvt L=1 W=2.5 nf=1 ad='int((nf+1)/2) * W/nf * 0.29' as='int((nf+2)/2) * W/nf * 0.29'
+ pd='2*int((nf+1)/2) * (W/nf + 0.29)' ps='2*int((nf+2)/2) * (W/nf + 0.29)' nrd='0.29 / W' nrs='0.29 / W'
+ sa=0 sb=0 sd=0 mult=2 m=2
XM23 Vb Vb net6 DD sky130_fd_pr__pfet_01v8_lvt L=2 W=2.5 nf=1 ad='int((nf+1)/2) * W/nf * 0.29' as='int((nf+2)/2) * W/nf * 0.29'
+ pd='2*int((nf+1)/2) * (W/nf + 0.29)' ps='2*int((nf+2)/2) * (W/nf + 0.29)' nrd='0.29 / W' nrs='0.29 / W'
+ sa=0 sb=0 sd=0 mult=2 m=2
XM1 DD DD DD DD sky130_fd_pr__pfet_01v8_lvt L=2 W=0.5 nf=1 ad='int((nf+1)/2) * W/nf * 0.29' as='int((nf+2)/2) * W/nf * 0.29'
+ pd='2*int((nf+1)/2) * (W/nf + 0.29)' ps='2*int((nf+2)/2) * (W/nf + 0.29)' nrd='0.29 / W' nrs='0.29 / W'
+ sa=0 sb=0 sd=0 mult=8 m=8
XM2 SS SS SS SS sky130_fd_pr__nfet_01v8_lvt L=1 W=2.5 nf=1 ad='int((nf+1)/2) * W/nf * 0.29' as='int((nf+2)/2) * W/nf * 0.29'
+ pd='2*int((nf+1)/2) * (W/nf + 0.29)' ps='2*int((nf+2)/2) * (W/nf + 0.29)' nrd='0.29 / W' nrs='0.29 / W'
+ sa=0 sb=0 sd=0 mult=2 m=2
.ends


* expanding   symbol:  iref_2nA_vref.sym # of pins=3
** sym_path: xschem/iref_2nA_vref.sym
** sch_path: xschem/iref_2nA_vref.sch
.subckt iref_2nA_vref VREF DD SS
*.iopin DD
*.iopin SS
*.iopin VREF
XM1 N2 N1 DD DD sky130_fd_pr__pfet_01v8 L=4.38 W=2.37 nf=1 ad='int((nf+1)/2) * W/nf * 0.29' as='int((nf+2)/2) * W/nf * 0.29'
+ pd='2*int((nf+1)/2) * (W/nf + 0.29)' ps='2*int((nf+2)/2) * (W/nf + 0.29)' nrd='0.29 / W' nrs='0.29 / W'
+ sa=0 sb=0 sd=0 mult=1 m=1
XM2 SS N2 N2 N2 sky130_fd_pr__pfet_01v8_lvt L=6.97 W=0.88 nf=1 ad='int((nf+1)/2) * W/nf * 0.29' as='int((nf+2)/2) * W/nf * 0.29'
+ pd='2*int((nf+1)/2) * (W/nf + 0.29)' ps='2*int((nf+2)/2) * (W/nf + 0.29)' nrd='0.29 / W' nrs='0.29 / W'
+ sa=0 sb=0 sd=0 mult=1 m=1
XM3 N1 DD DD DD sky130_fd_pr__pfet_01v8_lvt L=4 W=0.5 nf=1 ad='int((nf+1)/2) * W/nf * 0.29' as='int((nf+2)/2) * W/nf * 0.29'
+ pd='2*int((nf+1)/2) * (W/nf + 0.29)' ps='2*int((nf+2)/2) * (W/nf + 0.29)' nrd='0.29 / W' nrs='0.29 / W'
+ sa=0 sb=0 sd=0 mult=1 m=1
XM4 VREF N2 N1 DD sky130_fd_pr__pfet_01v8_lvt L=2.77 W=3.43 nf=1 ad='int((nf+1)/2) * W/nf * 0.29' as='int((nf+2)/2) * W/nf * 0.29'
+ pd='2*int((nf+1)/2) * (W/nf + 0.29)' ps='2*int((nf+2)/2) * (W/nf + 0.29)' nrd='0.29 / W' nrs='0.29 / W'
+ sa=0 sb=0 sd=0 mult=1 m=1
XM5 SS SS VREF VREF sky130_fd_pr__pfet_01v8 L=0.5 W=2 nf=1 ad='int((nf+1)/2) * W/nf * 0.29' as='int((nf+2)/2) * W/nf * 0.29'
+ pd='2*int((nf+1)/2) * (W/nf + 0.29)' ps='2*int((nf+2)/2) * (W/nf + 0.29)' nrd='0.29 / W' nrs='0.29 / W'
+ sa=0 sb=0 sd=0 mult=4 m=4
.ends

.end
